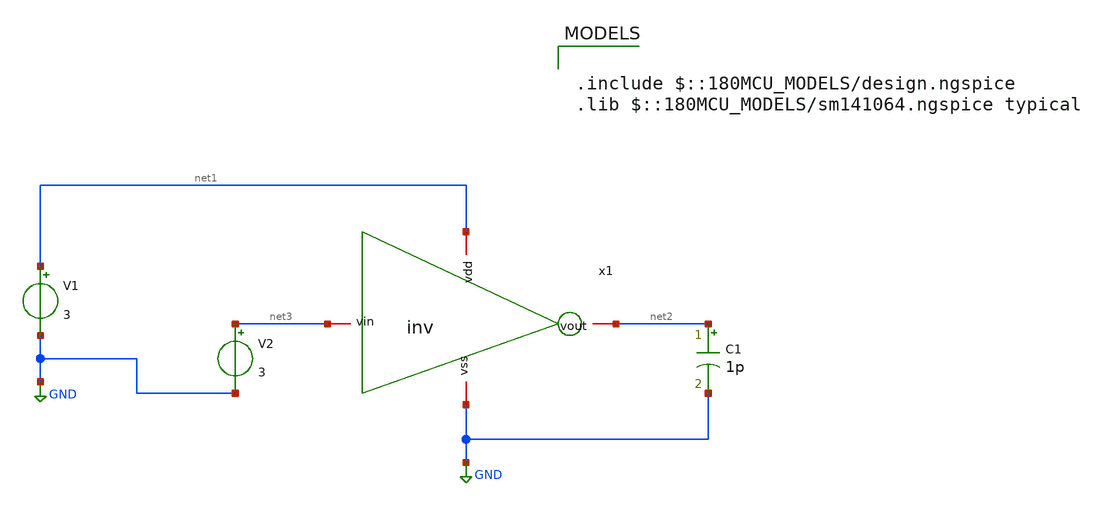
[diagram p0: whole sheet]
** sch_path: src/FullCust_files/INVTRAIL.sch
**.subckt INVTRAIL
x1 net1 net3 net2 GND inv
V1 net1 GND 3
V2 net3 GND 3
C1 net2 GND 1p m=1
**** begin user architecture code

.include $::180MCU_MODELS/design.ngspice
.lib $::180MCU_MODELS/sm141064.ngspice typical

**** end user architecture code
**.ends

* expanding   symbol:  pixel/inv.sym # of pins=4
** sym_path: src/Pixel/inv.sym
** sch_path: src/Pixel/inv.sch
.subckt inv vdd vin vout vss
*.iopin vin
*.iopin vout
*.iopin vdd
*.iopin vss
XM1 vout vin vss vss nfet_03v3 L=0.28u W=0.42u nf=1 ad='int((nf+1)/2) * W/nf * 0.18u' as='int((nf+2)/2) * W/nf * 0.18u'
+ pd='2*int((nf+1)/2) * (W/nf + 0.18u)' ps='2*int((nf+2)/2) * (W/nf + 0.18u)' nrd='0.18u / W' nrs='0.18u / W'
+ sa=0 sb=0 sd=0 m=1
XM2 vout vin vdd vdd pfet_03v3 L=0.28u W=0.84u nf=1 ad='int((nf+1)/2) * W/nf * 0.18u' as='int((nf+2)/2) * W/nf * 0.18u'
+ pd='2*int((nf+1)/2) * (W/nf + 0.18u)' ps='2*int((nf+2)/2) * (W/nf + 0.18u)' nrd='0.18u / W' nrs='0.18u / W'
+ sa=0 sb=0 sd=0 m=1
.ends

.GLOBAL GND
.end
